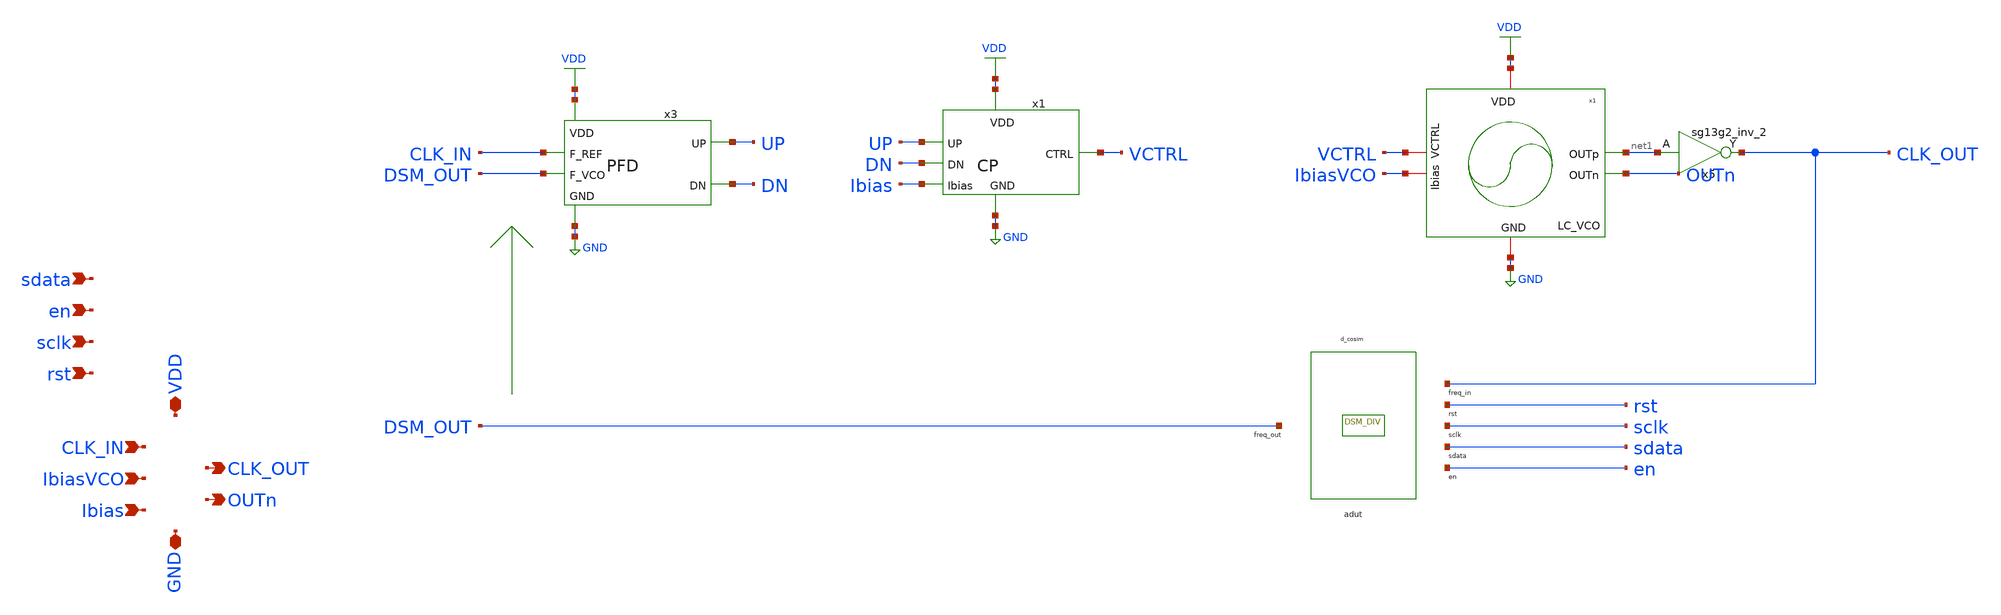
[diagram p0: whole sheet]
** sch_path: schematic/top-pll/LC_VCO_PLL_LVS.sch
**.subckt LC_VCO_PLL_LVS GND VDD CLK_IN IbiasVCO Ibias OUTn CLK_OUT sdata en sclk rst
*.iopin GND
*.iopin VDD
*.ipin CLK_IN
*.ipin IbiasVCO
*.ipin Ibias
*.opin OUTn
*.opin CLK_OUT
*.ipin sdata
*.ipin en
*.ipin sclk
*.ipin rst
x5 CLK_OUT net1 VDD GND sg13g2_inv_2
x1 VDD UP VCTRL DN GND Ibias CP
x2 VDD net1 OUTn IbiasVCO VCTRL GND LC_VCO
x3 VDD UP CLK_IN DSM_OUT DN GND PFD
adut [ CLK_OUT rst sclk sdata en ] [ DSM_OUT ] null dut
.model dut d_cosim simulation=./../dsm_and_freq_divider.so
**.ends
.GLOBAL VDD
.GLOBAL GND
.end
